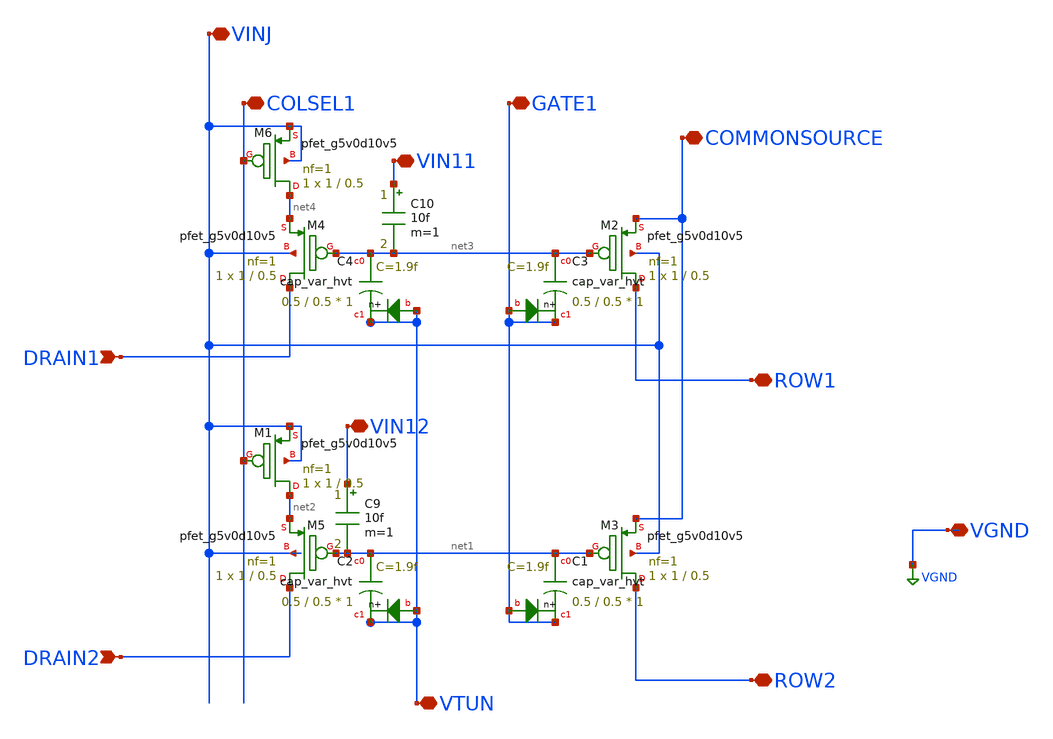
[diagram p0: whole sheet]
** sch_path: libs.ref/sky130_hilas_sc/xschem/sky130_hilas_FGBiasWeakGate2x1cell.sch
**.subckt sky130_hilas_FGBiasWeakGate2x1cell DRAIN1 DRAIN2 GATE1 VTUN COLSEL1 VINJ COMMONSOURCE ROW1
*+ ROW2 VIN11 VIN12 VGND
*.ipin DRAIN1
*.ipin DRAIN2
*.iopin GATE1
*.iopin VTUN
*.iopin COLSEL1
*.iopin VINJ
*.iopin COMMONSOURCE
*.iopin ROW1
*.iopin ROW2
*.iopin VIN11
*.iopin VIN12
*.iopin VGND
XM3 ROW2 net1 COMMONSOURCE VINJ sky130_fd_pr__pfet_g5v0d10v5 L=0.5 W=1 nf=1 ad='int((nf+1)/2) * W/nf * 0.29'
+ as='int((nf+2)/2) * W/nf * 0.29' pd='2*int((nf+1)/2) * (W/nf + 0.29)' ps='2*int((nf+2)/2) * (W/nf + 0.29)'
+ nrd='0.29 / W' nrs='0.29 / W' sa=0 sb=0 sd=0 mult=1 m=1
XC1 net1 GATE1 GATE1 sky130_fd_pr__cap_var_hvt W=0.5 L=0.5 VM=1 m=1
XM5 DRAIN2 net1 net2 VINJ sky130_fd_pr__pfet_g5v0d10v5 L=0.5 W=1 nf=1 ad='int((nf+1)/2) * W/nf * 0.29'
+ as='int((nf+2)/2) * W/nf * 0.29' pd='2*int((nf+1)/2) * (W/nf + 0.29)' ps='2*int((nf+2)/2) * (W/nf + 0.29)'
+ nrd='0.29 / W' nrs='0.29 / W' sa=0 sb=0 sd=0 mult=1 m=1
XC2 net1 VTUN VTUN sky130_fd_pr__cap_var_hvt W=0.5 L=0.5 VM=1 m=1
XM1 net2 COLSEL1 VINJ VINJ sky130_fd_pr__pfet_g5v0d10v5 L=0.5 W=1 nf=1 ad='int((nf+1)/2) * W/nf * 0.29'
+ as='int((nf+2)/2) * W/nf * 0.29' pd='2*int((nf+1)/2) * (W/nf + 0.29)' ps='2*int((nf+2)/2) * (W/nf + 0.29)'
+ nrd='0.29 / W' nrs='0.29 / W' sa=0 sb=0 sd=0 mult=1 m=1
XM2 ROW1 net3 COMMONSOURCE VINJ sky130_fd_pr__pfet_g5v0d10v5 L=0.5 W=1 nf=1 ad='int((nf+1)/2) * W/nf * 0.29'
+ as='int((nf+2)/2) * W/nf * 0.29' pd='2*int((nf+1)/2) * (W/nf + 0.29)' ps='2*int((nf+2)/2) * (W/nf + 0.29)'
+ nrd='0.29 / W' nrs='0.29 / W' sa=0 sb=0 sd=0 mult=1 m=1
XC3 net3 GATE1 GATE1 sky130_fd_pr__cap_var_hvt W=0.5 L=0.5 VM=1 m=1
XM4 DRAIN1 net3 net4 VINJ sky130_fd_pr__pfet_g5v0d10v5 L=0.5 W=1 nf=1 ad='int((nf+1)/2) * W/nf * 0.29'
+ as='int((nf+2)/2) * W/nf * 0.29' pd='2*int((nf+1)/2) * (W/nf + 0.29)' ps='2*int((nf+2)/2) * (W/nf + 0.29)'
+ nrd='0.29 / W' nrs='0.29 / W' sa=0 sb=0 sd=0 mult=1 m=1
XC4 net3 VTUN VTUN sky130_fd_pr__cap_var_hvt W=0.5 L=0.5 VM=1 m=1
XM6 net4 COLSEL1 VINJ VINJ sky130_fd_pr__pfet_g5v0d10v5 L=0.5 W=1 nf=1 ad='int((nf+1)/2) * W/nf * 0.29'
+ as='int((nf+2)/2) * W/nf * 0.29' pd='2*int((nf+1)/2) * (W/nf + 0.29)' ps='2*int((nf+2)/2) * (W/nf + 0.29)'
+ nrd='0.29 / W' nrs='0.29 / W' sa=0 sb=0 sd=0 mult=1 m=1
C9 VIN12 net1 10f m=1
C10 VIN11 net3 10f m=1
**.ends
.GLOBAL VGND
.end
